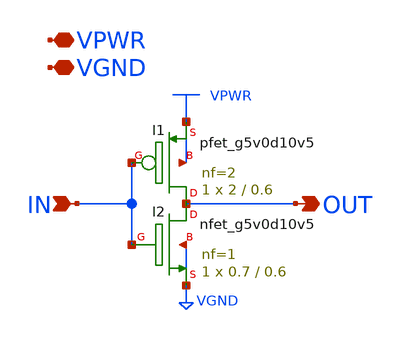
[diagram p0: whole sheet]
** sch_path: common/hvsbt_inv_x1.sch
* Copyright 2023 David Mitchell Bailey
* Licensed under the Apache License, Version 2.0 (the "License");
* you may not use this file except in compliance with the License.
* You may obtain a copy of the License at
* https://www.apache.org/licenses/LICENSE-2.0
* Unless required by applicable law or agreed to in writing, software
* distributed under the License is distributed on an "AS IS" BASIS,
* WITHOUT WARRANTIES OR CONDITIONS OF ANY KIND, either express or implied.
* See the License for the specific language governing permissions and
* limitations under the License.
**.subckt hvsbt_inv_x1 IN OUT VPWR VGND
*.ipin IN
*.opin OUT
*.iopin VPWR
*.iopin VGND
XI2 OUT IN VGND VGND sky130_fd_pr__nfet_g5v0d10v5 L=0.6 W=0.7 nf=1 ad='int((nf+1)/2) * W/nf * 0.29' as='int((nf+2)/2) * W/nf * 0.29'
+ pd='2*int((nf+1)/2) * (W/nf + 0.29)' ps='2*int((nf+2)/2) * (W/nf + 0.29)' nrd='0.29 / W' nrs='0.29 / W'
+ sa=0 sb=0 sd=0 mult=1 m=1
XI1 OUT IN VPWR VPWR sky130_fd_pr__pfet_g5v0d10v5 L=0.6 W=2 nf=2 ad='int((nf+1)/2) * W/nf * 0.29' as='int((nf+2)/2) * W/nf * 0.29'
+ pd='2*int((nf+1)/2) * (W/nf + 0.29)' ps='2*int((nf+2)/2) * (W/nf + 0.29)' nrd='0.29 / W' nrs='0.29 / W'
+ sa=0 sb=0 sd=0 mult=1 m=1
**.ends
.end
